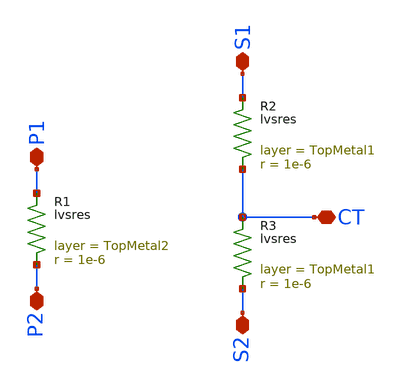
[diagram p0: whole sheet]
** sch_path: ihp-sg13g2/schematic/xschem/sg13_balun_lvsres_swap.sch
**.subckt sg13_balun_lvsres_swap P1 P2 S1 S2 CT
*.iopin P1
*.iopin P2
*.iopin S1
*.iopin S2
*.iopin CT
RR1 P1 P2 1e-6
RR2 S1 CT 1e-6
RR3 CT S2 1e-6
**.ends
.end
